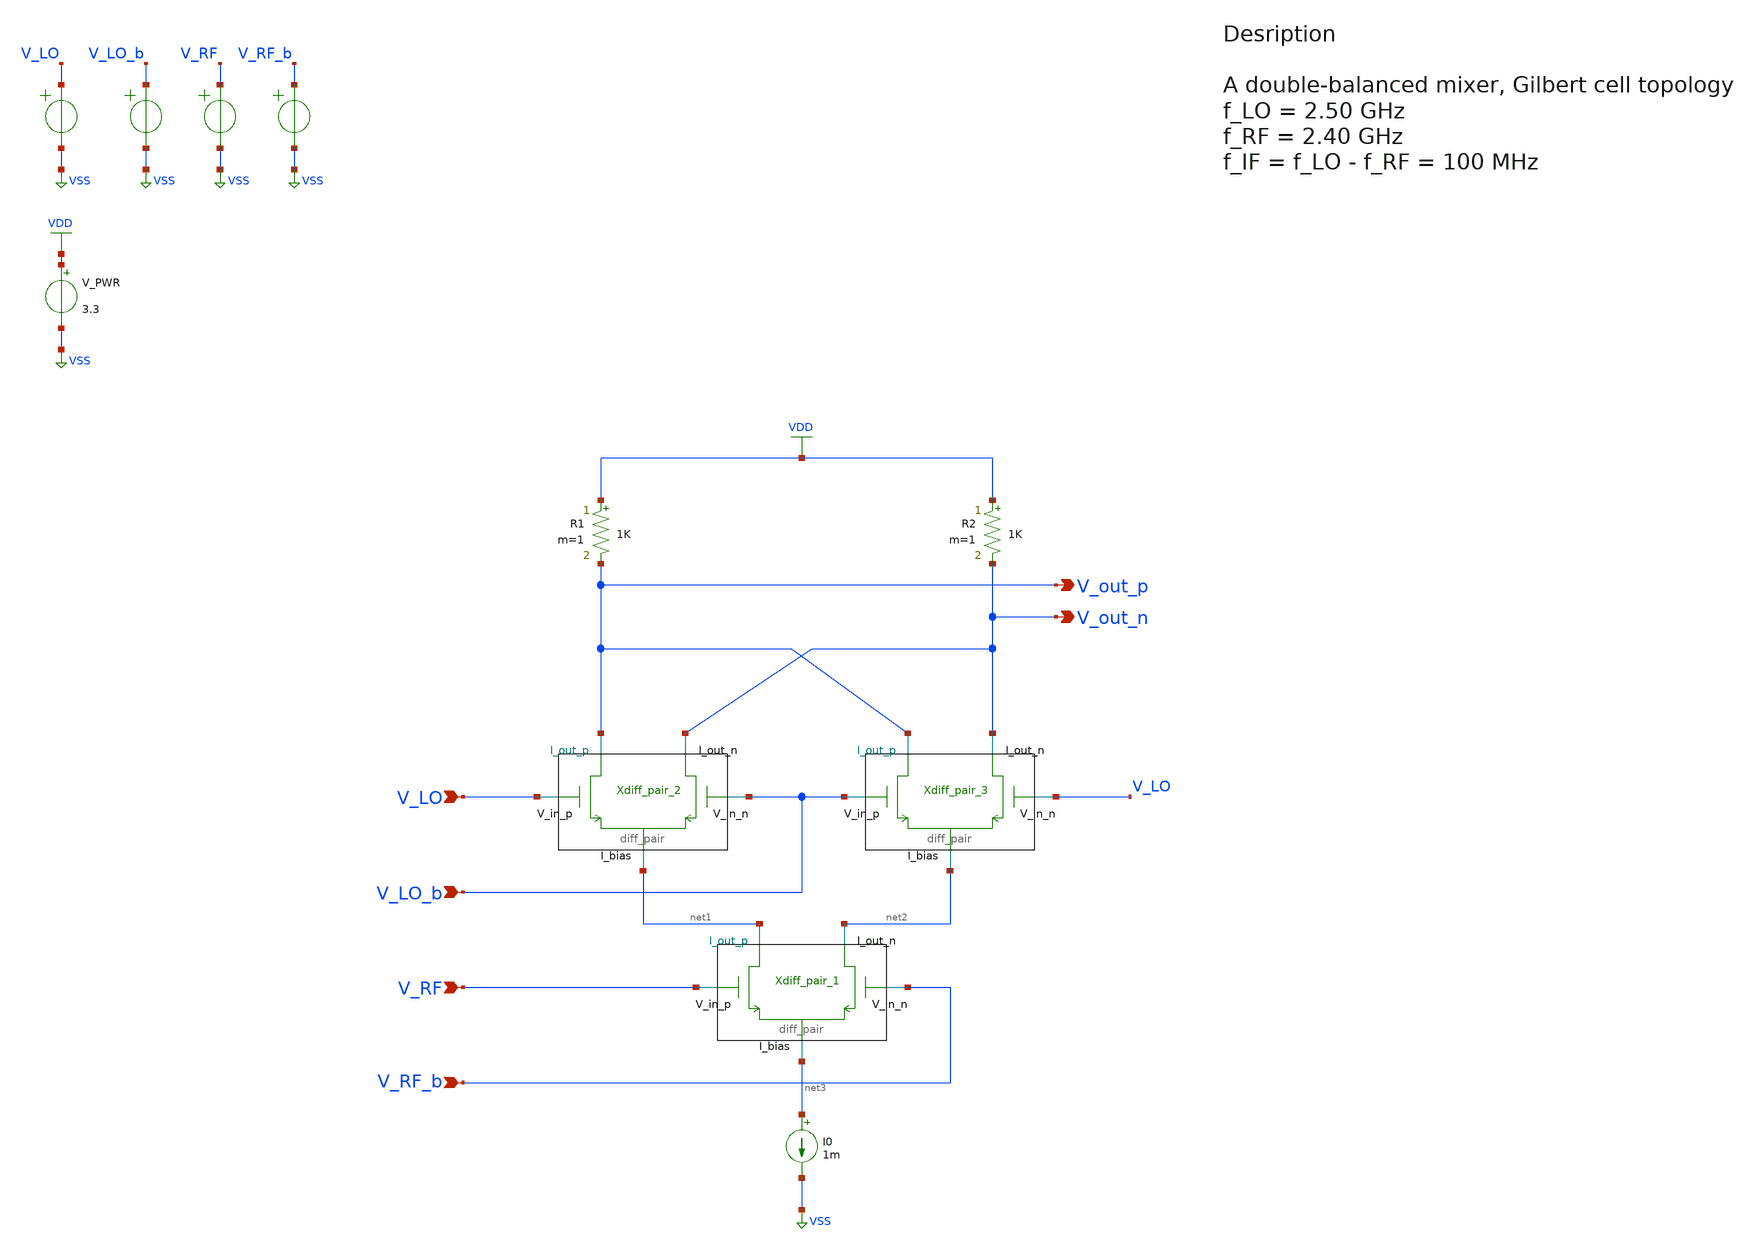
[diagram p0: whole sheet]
** sch_path: src/design_xsch/Gilbert_cell.sch
**.subckt Gilbert_cell V_LO V_LO_b V_RF V_RF_b V_out_p V_out_n
*.ipin V_LO
*.ipin V_LO_b
*.ipin V_RF
*.ipin V_RF_b
*.opin V_out_p
*.opin V_out_n
I0 net3 VSS 1m
E_LO V_LO VSS VOL=' '1' '
E_LO_b V_LO_b VSS VOL=' '1' '
E_RF V_RF VSS VOL=' '1' '
E_RF_b V_RF_b VSS VOL=' '1' '
Xdiff_pair_1 net2 net1 V_RF V_RF_b net3 VSS diff_pair W_neg=0.22u L_neg=0.28u W_pos=2u L_pos=0.28u
+ m=1
Xdiff_pair_2 V_out_n V_out_p V_LO V_LO_b net1 VSS diff_pair W_neg=0.22u L_neg=0.28u W_pos=0.22u
+ L_pos=0.28u m=1
Xdiff_pair_3 V_out_n V_out_p V_LO_b V_LO net2 VSS diff_pair W_neg=0.22u L_neg=0.28u W_pos=0.22u
+ L_pos=0.28u m=1
R1 VDD V_out_p 1K m=1
R2 VDD V_out_n 1K m=1
V_PWR VDD VSS 3.3
.save i(v_pwr)
**** begin user architecture code

.include $::180MCU_MODELS/design.ngspice
.lib $::180MCU_MODELS/sm141064.ngspice typical



.control
    * define frequencies
    let f_lo = 2.5e9
    let f_rf = 2.4e9
    let f_if = f_lo - f_rf

    save all

    alter @E_LO[VOL] = "'1.5 + 0.05*sin(2*pi*f_lo*TIME) + 0.05*sin(2*pi*f_lo*TIME)'"
    alter @E_LO_b[VOL] = "'1.5 - 0.05*sin(2*pi*f_lo*TIME) - 0.05*sin(2*pi*f_lo*TIME)'"
    alter @E_RF[VOL] = "'1.5 + 0.05*sin(2*pi*f_fr*TIME) + 0.05*sin(2*pi*f_fr*TIME)'"
    alter @E_RF_b[VOL] = "'1.5 + 0.05*sin(2*pi*f_fr*TIME) + 0.05*sin(2*pi*f_fr*TIME)'"

    * operating point
    op

    set appendwrite
    * Transient analysis to observe mixing operation
    tran 5p 50n
    write Gilbert_sim.raw
.endc


**** end user architecture code
**.ends

* expanding   symbol:  /home/vasil/Downloads/SSCS_PICO_2025/src/design_xsch/diff_pair.sym # of
*+ pins=5
** sym_path: src/design_xsch/diff_pair.sym
** sch_path: src/design_xsch/diff_pair.sch
.subckt diff_pair I_out_n I_out_p V_in_p V_in_n I_bias VSSPIN  mult=1  W_neg=0.22u L_neg=0.28u
+ W_pos=0.22u L_pos=0.28u
*.ipin V_in_p
*.ipin V_in_n
*.iopin I_out_p
*.iopin I_out_n
*.iopin I_bias
XM1 I_out_p V_in_p I_bias VSS nfet_03v3 L=L_pos W=W_pos nf=1 ad='int((nf+1)/2) * W/nf * 0.18u' as='int((nf+2)/2) * W/nf * 0.18u'
+ pd='2*int((nf+1)/2) * (W/nf + 0.18u)' ps='2*int((nf+2)/2) * (W/nf + 0.18u)' nrd='0.18u / W' nrs='0.18u / W'
+ sa=0 sb=0 sd=0 m=mult
XM2 I_out_n V_in_n I_bias VSS nfet_03v3 L=L_neg W=W_neg nf=1 ad='int((nf+1)/2) * W/nf * 0.18u' as='int((nf+2)/2) * W/nf * 0.18u'
+ pd='2*int((nf+1)/2) * (W/nf + 0.18u)' ps='2*int((nf+2)/2) * (W/nf + 0.18u)' nrd='0.18u / W' nrs='0.18u / W'
+ sa=0 sb=0 sd=0 m=mult
.ends

.GLOBAL VSS
.GLOBAL VDD
.end
